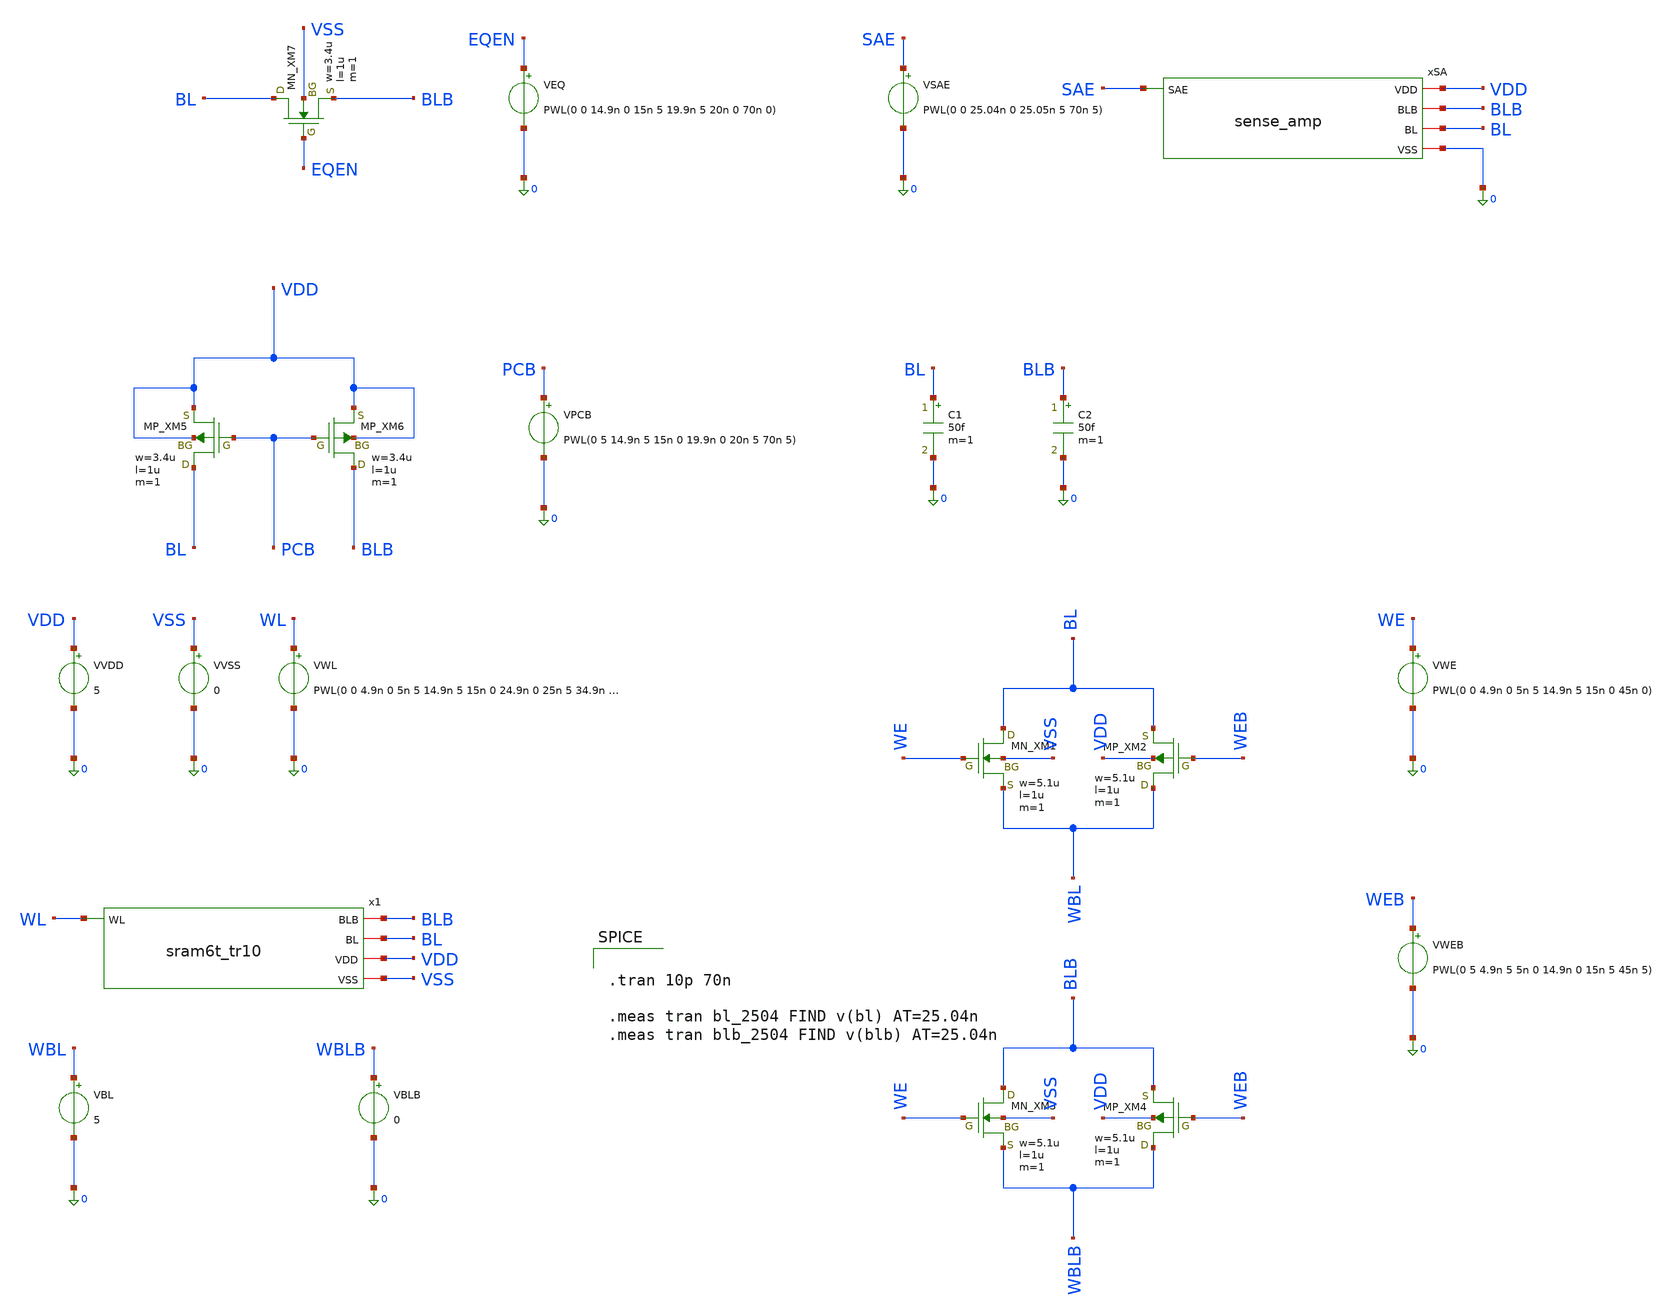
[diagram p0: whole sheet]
** sch_path: cell/tb_read_sense.sch
**.subckt tb_read_sense
VVDD VDD 0 5
VWL WL 0 PWL(0 0 4.9n 0 5n 5 14.9n 5 15n 0 24.9n 0 25n 5 34.9n 5 35n 0 70n 0)
VBL WBL 0 5
VBLB WBLB 0 0
VVSS VSS 0 0
x1 BL BLB WL VDD VSS sram6t_tr10
XXM1 BL WE WBL VSS NMOS w=5.1u l=1u nrd=0 nrs=0 m=1
XXM2 WBL WEB BL VDD PMOS w=5.1u l=1u nrd=0 nrs=0 m=1
VWE WE 0 PWL(0 0 4.9n 0 5n 5 14.9n 5 15n 0 45n 0)
VWEB WEB 0 PWL(0 5 4.9n 5 5n 0 14.9n 0 15n 5 45n 5)
XXM3 BLB WE WBLB VSS NMOS w=5.1u l=1u nrd=0 nrs=0 m=1
XXM4 WBLB WEB BLB VDD PMOS w=5.1u l=1u nrd=0 nrs=0 m=1
XXM5 BL PCB VDD VDD PMOS w=3.4u l=1u nrd=0 nrs=0 m=1
XXM6 BLB PCB VDD VDD PMOS w=3.4u l=1u nrd=0 nrs=0 m=1
VPCB PCB 0 PWL(0 5 14.9n 5 15n 0 19.9n 0 20n 5 70n 5)
C1 BL 0 50f m=1
C2 BLB 0 50f m=1
XXM7 BL EQEN BLB VSS NMOS w=3.4u l=1u nrd=0 nrs=0 m=1
VEQ EQEN 0 PWL(0 0 14.9n 0 15n 5 19.9n 5 20n 0 70n 0)
xSA VDD BLB BL SAE 0 sense_amp
VSAE SAE 0 PWL(0 0 25.04n 0 25.05n 5 70n 5)
**** begin user architecture code
 .include $::LIB/ip62_models


.tran 10p 70n

.meas tran bl_2504 FIND v(bl) AT=25.04n
.meas tran blb_2504 FIND v(blb) AT=25.04n


**** end user architecture code
**.ends
.end
